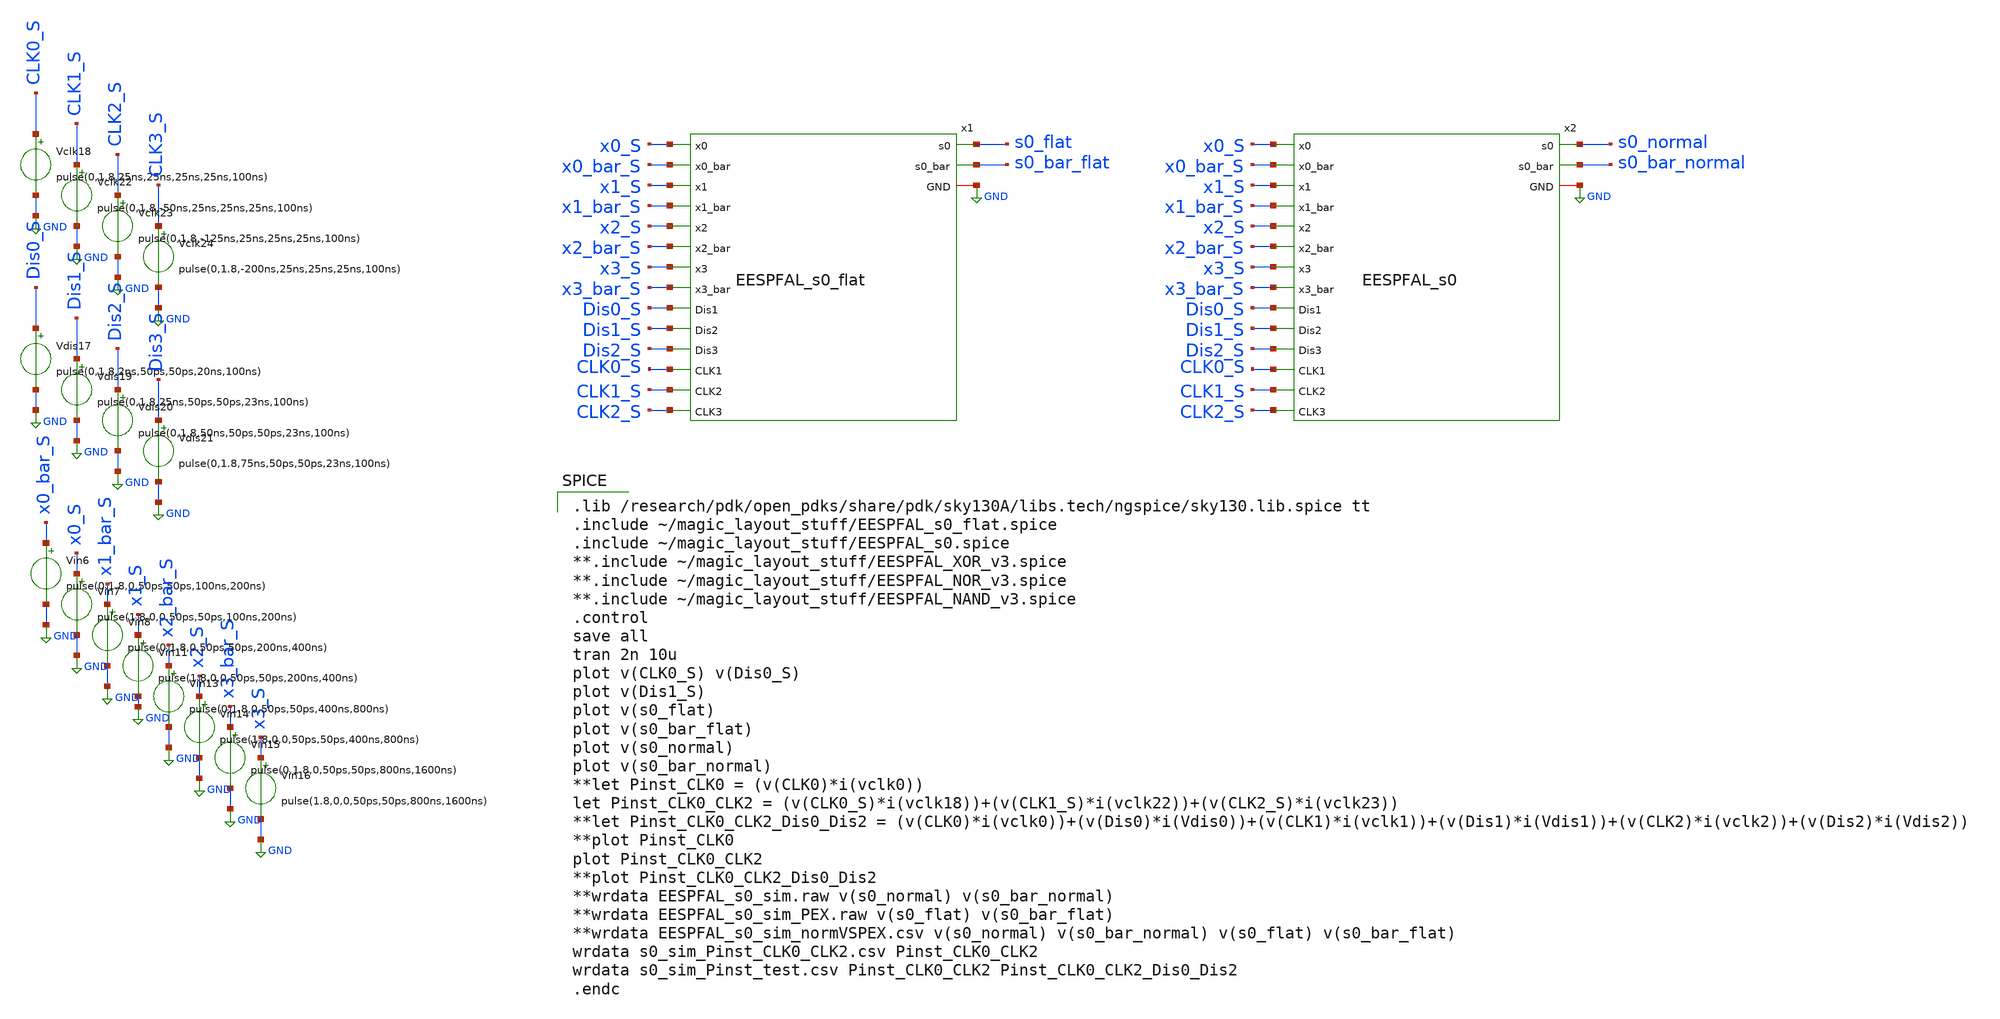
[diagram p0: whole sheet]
** sch_path: skywater_stuff/EESPFAL_s0_sim.sch
**.subckt EESPFAL_s0_sim
x1 GND x0_S x0_bar_S x1_S x1_bar_S x2_S x2_bar_S x3_S x3_bar_S Dis0_S Dis1_S Dis2_S s0_flat
+ s0_bar_flat CLK2_S CLK1_S CLK0_S EESPFAL_s0_flat
Vin6 x0_bar_S GND pulse(0,1.8,0,50ps,50ps,100ns,200ns)
Vin7 x0_S GND pulse(1.8,0,0,50ps,50ps,100ns,200ns)
Vin8 x1_bar_S GND pulse(0,1.8,0,50ps,50ps,200ns,400ns)
Vin11 x1_S GND pulse(1.8,0,0,50ps,50ps,200ns,400ns)
Vin13 x2_bar_S GND pulse(0,1.8,0,50ps,50ps,400ns,800ns)
Vin14 x2_S GND pulse(1.8,0,0,50ps,50ps,400ns,800ns)
Vin15 x3_bar_S GND pulse(0,1.8,0,50ps,50ps,800ns,1600ns)
Vin16 x3_S GND pulse(1.8,0,0,50ps,50ps,800ns,1600ns)
Vdis17 Dis0_S GND pulse(0,1.8,2ns,50ps,50ps,20ns,100ns)
Vclk18 CLK0_S GND pulse(0,1.8,25ns,25ns,25ns,25ns,100ns)
Vdis19 Dis1_S GND pulse(0,1.8,25ns,50ps,50ps,23ns,100ns)
Vdis20 Dis2_S GND pulse(0,1.8,50ns,50ps,50ps,23ns,100ns)
Vdis21 Dis3_S GND pulse(0,1.8,75ns,50ps,50ps,23ns,100ns)
Vclk22 CLK1_S GND pulse(0,1.8,-50ns,25ns,25ns,25ns,100ns)
Vclk23 CLK2_S GND pulse(0,1.8,-125ns,25ns,25ns,25ns,100ns)
Vclk24 CLK3_S GND pulse(0,1.8,-200ns,25ns,25ns,25ns,100ns)
x2 GND x0_S x0_bar_S x1_S x1_bar_S x2_S x2_bar_S x3_S x3_bar_S CLK0_S Dis0_S CLK2_S Dis1_S CLK1_S
+ Dis2_S s0_normal s0_bar_normal EESPFAL_s0
**** begin user architecture code

.lib /research/pdk/open_pdks/share/pdk/sky130A/libs.tech/ngspice/sky130.lib.spice tt
.include ~/magic_layout_stuff/EESPFAL_s0_flat.spice
.include ~/magic_layout_stuff/EESPFAL_s0.spice
**.include ~/magic_layout_stuff/EESPFAL_XOR_v3.spice
**.include ~/magic_layout_stuff/EESPFAL_NOR_v3.spice
**.include ~/magic_layout_stuff/EESPFAL_NAND_v3.spice
.control
save all
tran 2n 10u
plot v(CLK0_S) v(Dis0_S)
plot v(Dis1_S)
plot v(s0_flat)
plot v(s0_bar_flat)
plot v(s0_normal)
plot v(s0_bar_normal)
**let Pinst_CLK0 = (v(CLK0)*i(vclk0))
let Pinst_CLK0_CLK2 = (v(CLK0_S)*i(vclk18))+(v(CLK1_S)*i(vclk22))+(v(CLK2_S)*i(vclk23))
**let Pinst_CLK0_CLK2_Dis0_Dis2 =
*+ (v(CLK0)*i(vclk0))+(v(Dis0)*i(Vdis0))+(v(CLK1)*i(vclk1))+(v(Dis1)*i(Vdis1))+(v(CLK2)*i(vclk2))+(v(Dis2)*i(Vdis2))
**plot Pinst_CLK0
plot Pinst_CLK0_CLK2
**plot Pinst_CLK0_CLK2_Dis0_Dis2
**wrdata EESPFAL_s0_sim.raw v(s0_normal) v(s0_bar_normal)
**wrdata EESPFAL_s0_sim_PEX.raw v(s0_flat) v(s0_bar_flat)
**wrdata EESPFAL_s0_sim_normVSPEX.csv v(s0_normal) v(s0_bar_normal) v(s0_flat) v(s0_bar_flat)
wrdata s0_sim_Pinst_CLK0_CLK2.csv Pinst_CLK0_CLK2
wrdata s0_sim_Pinst_test.csv Pinst_CLK0_CLK2 Pinst_CLK0_CLK2_Dis0_Dis2
.endc


**** end user architecture code
**.ends
.GLOBAL GND
.end
